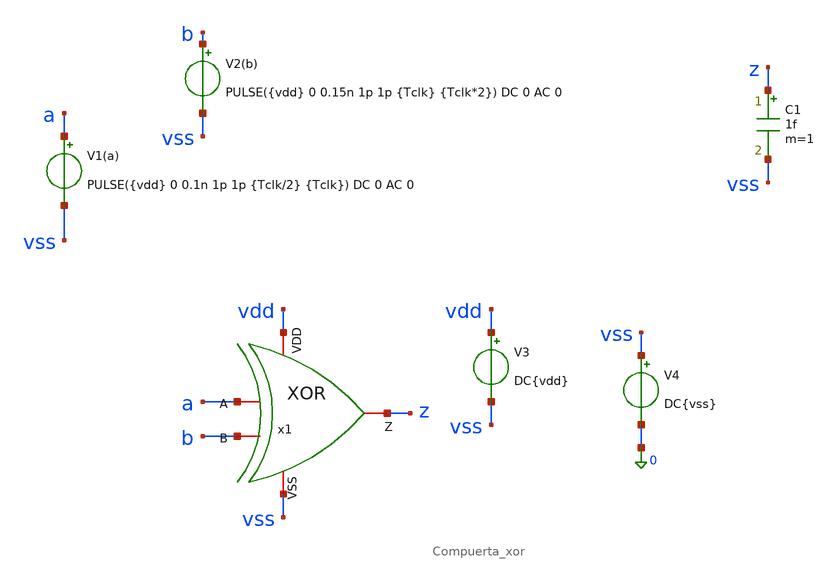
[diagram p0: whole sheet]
** sch_path: verification/testbenches/tb_xor.sch
**.subckt tb_xor
x1 vdd z b vss a Compuerta_xor
V1(a) a vss PULSE({vdd} 0 0.1n 1p 1p {Tclk/2} {Tclk}) DC 0 AC 0
V2(b) b vss PULSE({vdd} 0 0.15n 1p 1p {Tclk} {Tclk*2}) DC 0 AC 0
V3 vdd vss DC{vdd}
V4 vss 0 DC{vss}
C1 z vss 1f m=1
**** begin user architecture code


* Circuit Parameters
.param vdd = 1.2
.param vss = 0.0
.param Tclk = 10n
.options TEMP = 27.0
* Include Models - IHP SG13G2
.lib cornerMOSlv.lib mos_tt
* OP Parameters & Singals to save
.save all
*Simulations
.control
tran 0.01u 100n
setplot tran1
plot v(a) v(b)+1.5 v(z)+3
set filetype = ascii
write dcsweep.raw
.endc
.end


**** end user architecture code
**.ends
.end
